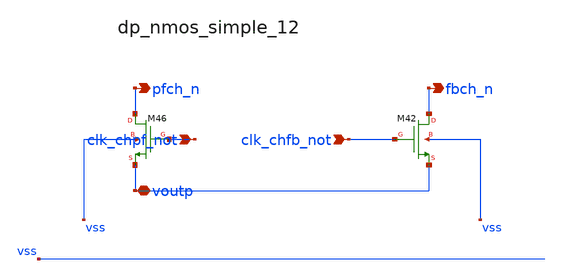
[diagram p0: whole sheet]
** sch_path: analog-db/raw/ia_003_fan_chopper_pf/hier/blocks/dp_nmos_simple_12.sch
**.subckt dp_nmos_simple_12 clk_chpf_not clk_chfb_not voutp pfch_n fbch_n
*.ipin clk_chpf_not
*.ipin clk_chfb_not
*.iopin voutp
*.opin pfch_n
*.opin fbch_n
XM42 fbch_n clk_chfb_not voutp vss sg13_lv_nmos w=x_dut_xm42_w l=x_dut_xm42_l ng=1 m=x_dut_xm42_m
XM46 pfch_n clk_chpf_not voutp vss sg13_lv_nmos w=x_dut_xm46_w l=x_dut_xm46_l ng=1 m=x_dut_xm46_m
**.ends
.end
